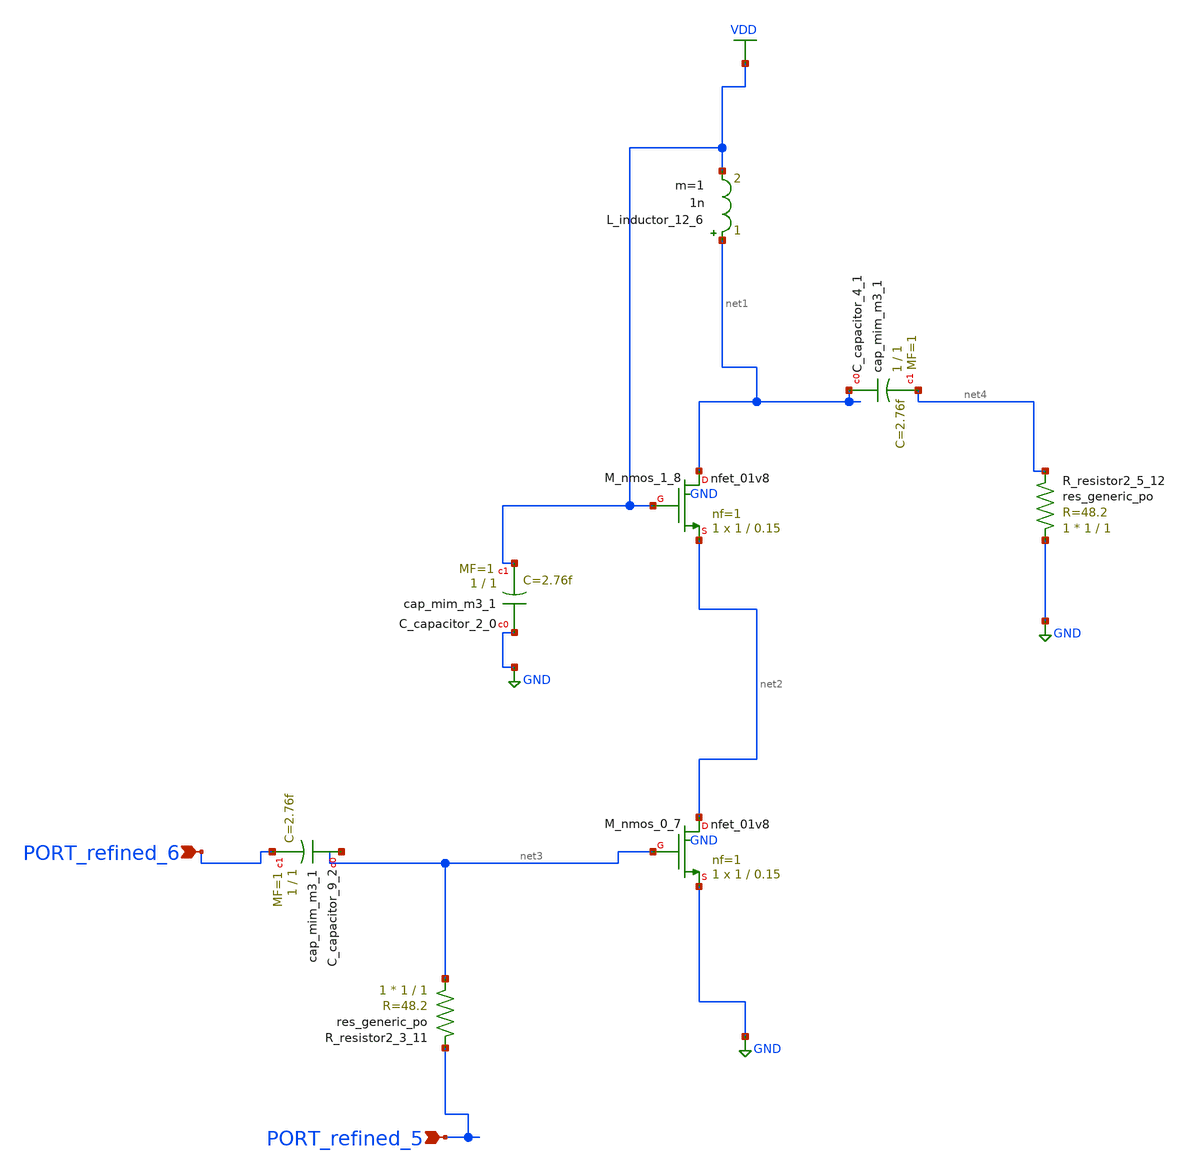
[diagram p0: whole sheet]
** sch_path: schematics/10_37649_AJES-25-014_08_001.sch
**.subckt 10_37649_AJES-25-014_08_001 PORT_refined_5 PORT_refined_6
*.ipin PORT_refined_5
*.ipin PORT_refined_6
XC_capacitor_2_0 GND VDD sky130_fd_pr__cap_mim_m3_1 W=1 L=1 MF=1 m=1
XC_capacitor_4_1 net1 net4 sky130_fd_pr__cap_mim_m3_1 W=1 L=1 MF=1 m=1
XC_capacitor_9_2 net3 PORT_refined_6 sky130_fd_pr__cap_mim_m3_1 W=1 L=1 MF=1 m=1
L_inductor_12_6 net1 VDD 1n m=1
XM_nmos_0_7 net2 net3 GND GND sky130_fd_pr__nfet_01v8 L=0.15 W=1 nf=1 ad='int((1 + 1)/2) * 1 / 1 * 0.29'
+ as='int((1 + 2)/2) * 1 / 1 * 0.29' pd='2*int((1 + 1)/2) * (1 / 1 + 0.29)' ps='2*int((1 + 2)/2) * (1 / 1 + 0.29)'
+ nrd='0.29 / 1 ' nrs='0.29 / 1 ' sa=0 sb=0 sd=0 mult=1 m=1
XM_nmos_1_8 net1 VDD net2 GND sky130_fd_pr__nfet_01v8 L=0.15 W=1 nf=1 ad='int((1 + 1)/2) * 1 / 1 * 0.29'
+ as='int((1 + 2)/2) * 1 / 1 * 0.29' pd='2*int((1 + 1)/2) * (1 / 1 + 0.29)' ps='2*int((1 + 2)/2) * (1 / 1 + 0.29)'
+ nrd='0.29 / 1 ' nrs='0.29 / 1 ' sa=0 sb=0 sd=0 mult=1 m=1
XR_resistor2_3_11 net3 PORT_refined_5 sky130_fd_pr__res_generic_po W=1 L=1 m=1
XR_resistor2_5_12 GND net4 sky130_fd_pr__res_generic_po W=1 L=1 m=1
**.ends
.GLOBAL GND
.GLOBAL VDD
.end
